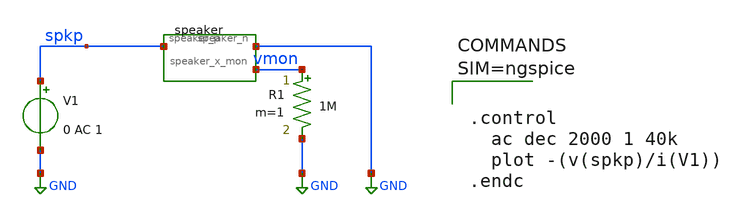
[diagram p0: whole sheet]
** sch_path: examples/analog_speaker/circuit.sch
**.subckt circuit
Xspeaker1 spkp GND vmon speaker
V1 spkp GND 0 AC 1
R1 vmon GND 1M m=1
**** begin user architecture code



.control
  ac dec 2000 1 40k
  plot -(v(spkp)/i(V1))
.endc



**** end user architecture code
**.ends

* expanding   symbol:  speaker.sym # of pins=3
** sym_path: examples/analog_speaker/speaker.sym
.include /workspace/speaker.spice
.GLOBAL GND
.end
